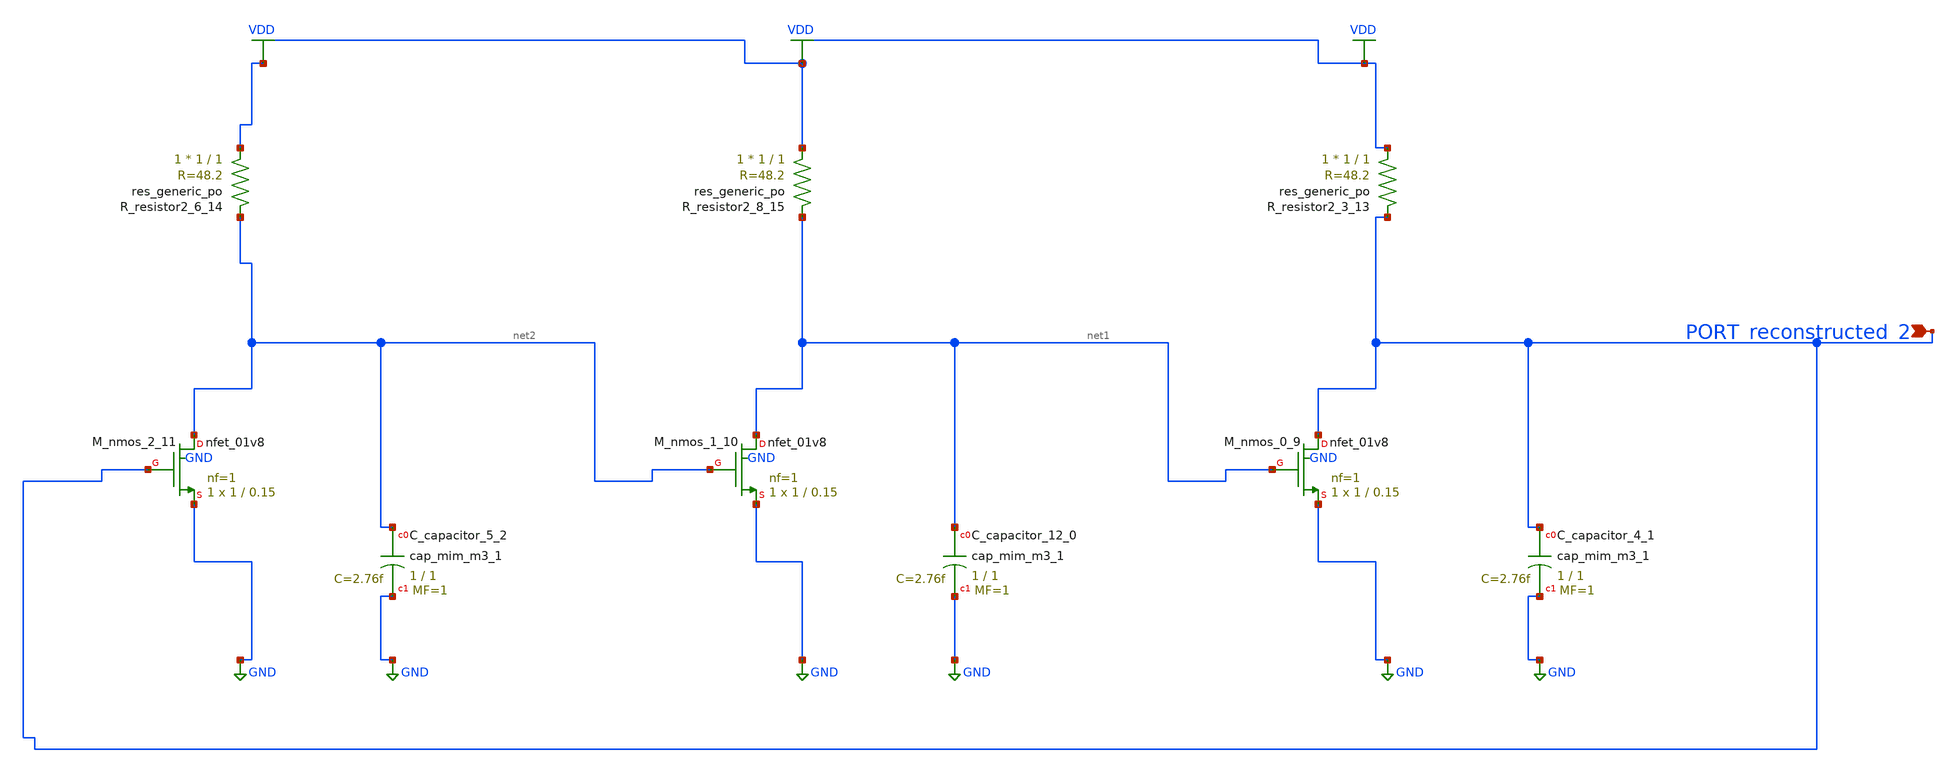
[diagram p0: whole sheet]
** sch_path: schematics/AMSNet/821.sch
**.subckt 821 PORT_reconstructed_2
*.ipin PORT_reconstructed_2
XC_capacitor_12_0 net1 GND sky130_fd_pr__cap_mim_m3_1 W=1 L=1 MF=1 m=1
XC_capacitor_4_1 PORT_reconstructed_2 GND sky130_fd_pr__cap_mim_m3_1 W=1 L=1 MF=1 m=1
XC_capacitor_5_2 net2 GND sky130_fd_pr__cap_mim_m3_1 W=1 L=1 MF=1 m=1
XM_nmos_0_9 PORT_reconstructed_2 net1 GND GND sky130_fd_pr__nfet_01v8 L=0.15 W=1 nf=1 ad='int((1 + 1)/2) * 1 / 1 * 0.29'
+ as='int((1 + 2)/2) * 1 / 1 * 0.29' pd='2*int((1 + 1)/2) * (1 / 1 + 0.29)' ps='2*int((1 + 2)/2) * (1 / 1 + 0.29)'
+ nrd='0.29 / 1 ' nrs='0.29 / 1 ' sa=0 sb=0 sd=0 mult=1 m=1
XM_nmos_1_10 net1 net2 GND GND sky130_fd_pr__nfet_01v8 L=0.15 W=1 nf=1 ad='int((1 + 1)/2) * 1 / 1 * 0.29'
+ as='int((1 + 2)/2) * 1 / 1 * 0.29' pd='2*int((1 + 1)/2) * (1 / 1 + 0.29)' ps='2*int((1 + 2)/2) * (1 / 1 + 0.29)'
+ nrd='0.29 / 1 ' nrs='0.29 / 1 ' sa=0 sb=0 sd=0 mult=1 m=1
XM_nmos_2_11 net2 PORT_reconstructed_2 GND GND sky130_fd_pr__nfet_01v8 L=0.15 W=1 nf=1 ad='int((1 + 1)/2) * 1 / 1 * 0.29'
+ as='int((1 + 2)/2) * 1 / 1 * 0.29' pd='2*int((1 + 1)/2) * (1 / 1 + 0.29)' ps='2*int((1 + 2)/2) * (1 / 1 + 0.29)'
+ nrd='0.29 / 1 ' nrs='0.29 / 1 ' sa=0 sb=0 sd=0 mult=1 m=1
XR_resistor2_3_13 VDD PORT_reconstructed_2 sky130_fd_pr__res_generic_po W=1 L=1 m=1
XR_resistor2_6_14 VDD net2 sky130_fd_pr__res_generic_po W=1 L=1 m=1
XR_resistor2_8_15 VDD net1 sky130_fd_pr__res_generic_po W=1 L=1 m=1
**.ends
.GLOBAL GND
.GLOBAL VDD
.end
